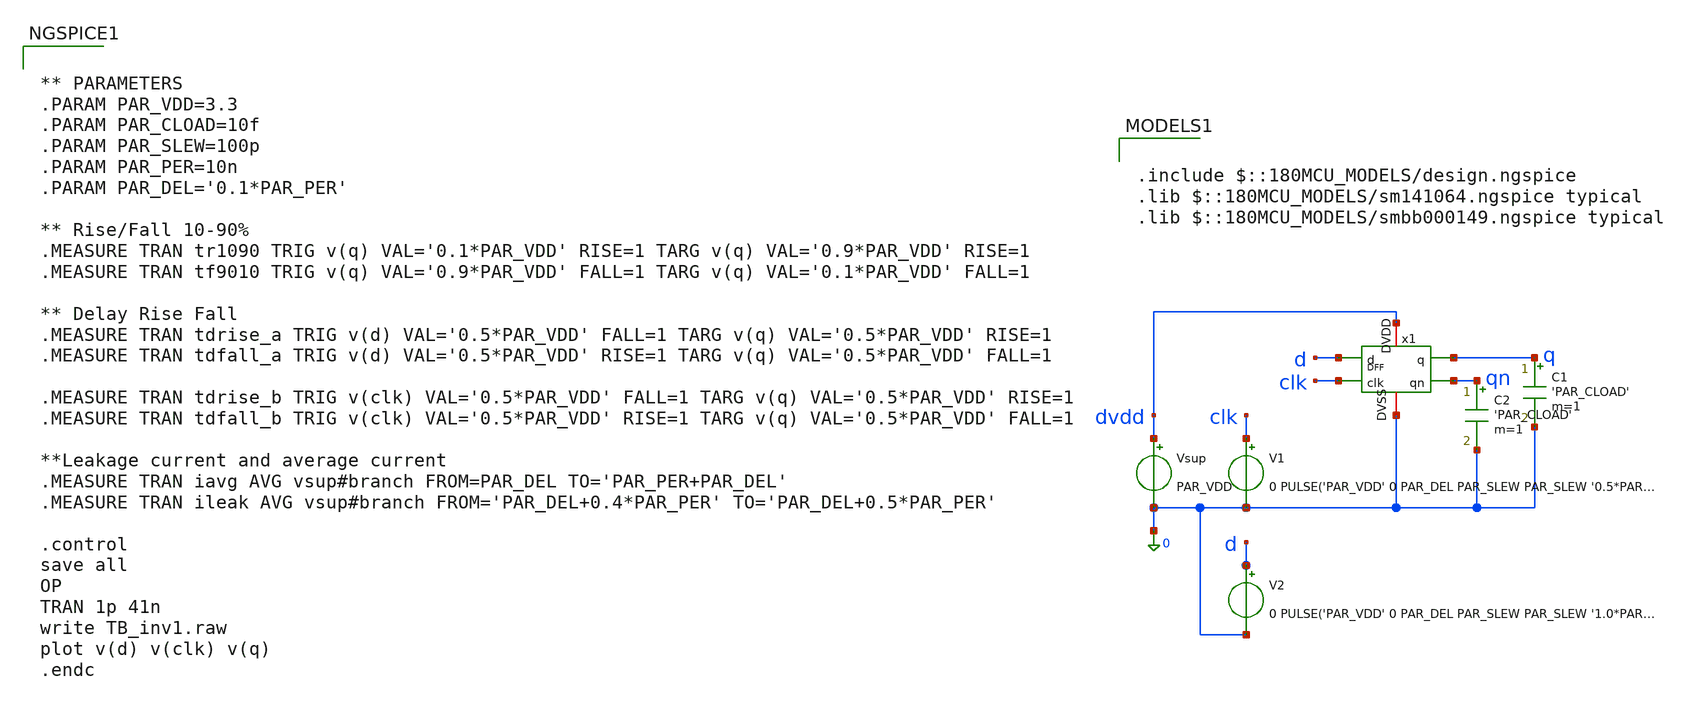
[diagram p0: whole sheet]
** sch_path: src/schematic/DFF/TB_DFF.sch
**.subckt TB_DFF
V1 clk 0 0 PULSE('PAR_VDD' 0 PAR_DEL PAR_SLEW PAR_SLEW '0.5*PAR_PER' '1.0*PAR_PER')
Vsup dvdd 0 PAR_VDD
C1 q 0 'PAR_CLOAD' m=1
V2 d 0 0 PULSE('PAR_VDD' 0 PAR_DEL PAR_SLEW PAR_SLEW '1.0*PAR_PER' '2.0*PAR_PER')
C2 qn 0 'PAR_CLOAD' m=1
x1 d q clk dvdd qn 0 DFF
**** begin user architecture code

.include $::180MCU_MODELS/design.ngspice
.lib $::180MCU_MODELS/sm141064.ngspice typical
.lib $::180MCU_MODELS/smbb000149.ngspice typical



** PARAMETERS
.PARAM PAR_VDD=3.3
.PARAM PAR_CLOAD=10f
.PARAM PAR_SLEW=100p
.PARAM PAR_PER=10n
.PARAM PAR_DEL='0.1*PAR_PER'

** Rise/Fall 10-90%
.MEASURE TRAN tr1090 TRIG v(q) VAL='0.1*PAR_VDD' RISE=1 TARG v(q) VAL='0.9*PAR_VDD' RISE=1
.MEASURE TRAN tf9010 TRIG v(q) VAL='0.9*PAR_VDD' FALL=1 TARG v(q) VAL='0.1*PAR_VDD' FALL=1

** Delay Rise Fall
.MEASURE TRAN tdrise_a TRIG v(d) VAL='0.5*PAR_VDD' FALL=1 TARG v(q) VAL='0.5*PAR_VDD' RISE=1
.MEASURE TRAN tdfall_a TRIG v(d) VAL='0.5*PAR_VDD' RISE=1 TARG v(q) VAL='0.5*PAR_VDD' FALL=1

.MEASURE TRAN tdrise_b TRIG v(clk) VAL='0.5*PAR_VDD' FALL=1 TARG v(q) VAL='0.5*PAR_VDD' RISE=1
.MEASURE TRAN tdfall_b TRIG v(clk) VAL='0.5*PAR_VDD' RISE=1 TARG v(q) VAL='0.5*PAR_VDD' FALL=1

**Leakage current and average current
.MEASURE TRAN iavg AVG vsup#branch FROM=PAR_DEL TO='PAR_PER+PAR_DEL'
.MEASURE TRAN ileak AVG vsup#branch FROM='PAR_DEL+0.4*PAR_PER' TO='PAR_DEL+0.5*PAR_PER'

.control
save all
OP
TRAN 1p 41n
write TB_inv1.raw
plot v(d) v(clk) v(q)
.endc


**** end user architecture code
**.ends

* expanding   symbol:  Chipaton2026/src/schematic/DFF/DFF.sym # of pins=6
** sym_path: src/schematic/DFF/DFF.sym
** sch_path: src/schematic/DFF/DFF.sch
.subckt DFF d q clk DVDD qn DVSS
*.ipin d
*.ipin clk
*.iopin DVDD
*.iopin DVSS
*.opin q
*.opin qn
x1 d net3 net1 DVDD net4 DVSS DLATCH
x2 DVDD clk net1 DVSS Inv1
x3 net3 q net2 DVDD qn DVSS DLATCH
x4 DVDD net1 net2 DVSS Inv1
* noconn #net4
.ends


* expanding   symbol:  src/schematic/DLATCH/DLATCH.sym # of pins=6
** sym_path: src/schematic/DLATCH/DLATCH.sym
** sch_path: src/schematic/DLATCH/DLATCH.sch
.subckt DLATCH d q e DVDD qn DVSS
*.ipin d
*.ipin e
*.iopin DVDD
*.iopin DVSS
*.opin q
*.opin qn
x1 DVDD net2 d e DVSS NAND
x2 DVDD net3 e net1 DVSS NAND
x3 DVDD q net2 qn DVSS NAND
x4 DVDD qn q net3 DVSS NAND
x5 DVDD d net1 DVSS Inv1
.ends


* expanding   symbol:  src/schematic/INV/Inv1.sym # of pins=4
** sym_path: src/schematic/INV/Inv1.sym
** sch_path: src/schematic/INV/Inv1.sch
.subckt Inv1 DVDD vin vout DVSS
*.ipin vin
*.opin vout
*.iopin DVDD
*.iopin DVSS
XM3 vout vin DVDD DVDD pfet_03v3 L=0.3u W=1.7u nf=1 ad='int((nf+1)/2) * W/nf * 0.18u' as='int((nf+2)/2) * W/nf * 0.18u'
+ pd='2*int((nf+1)/2) * (W/nf + 0.18u)' ps='2*int((nf+2)/2) * (W/nf + 0.18u)' nrd='0.18u / W' nrs='0.18u / W'
+ sa=0 sb=0 sd=0 m=1
XM4 vout vin DVSS DVSS nfet_03v3 L=0.3u W=0.85u nf=1 ad='int((nf+1)/2) * W/nf * 0.18u' as='int((nf+2)/2) * W/nf * 0.18u'
+ pd='2*int((nf+1)/2) * (W/nf + 0.18u)' ps='2*int((nf+2)/2) * (W/nf + 0.18u)' nrd='0.18u / W' nrs='0.18u / W'
+ sa=0 sb=0 sd=0 m=1
.ends


* expanding   symbol:  src/schematic/NAND/NAND.sym # of pins=5
** sym_path: src/schematic/NAND/NAND.sym
** sch_path: src/schematic/NAND/NAND.sch
.subckt NAND DVDD vout a b DVSS
*.ipin a
*.opin vout
*.iopin DVDD
*.iopin DVSS
*.ipin b
XM3 vout a DVDD DVDD pfet_03v3 L=0.3u W=1.7u nf=1 ad='int((nf+1)/2) * W/nf * 0.18u' as='int((nf+2)/2) * W/nf * 0.18u'
+ pd='2*int((nf+1)/2) * (W/nf + 0.18u)' ps='2*int((nf+2)/2) * (W/nf + 0.18u)' nrd='0.18u / W' nrs='0.18u / W'
+ sa=0 sb=0 sd=0 m=1
XM4 vout a net1 DVSS nfet_03v3 L=0.3u W=0.85u nf=1 ad='int((nf+1)/2) * W/nf * 0.18u' as='int((nf+2)/2) * W/nf * 0.18u'
+ pd='2*int((nf+1)/2) * (W/nf + 0.18u)' ps='2*int((nf+2)/2) * (W/nf + 0.18u)' nrd='0.18u / W' nrs='0.18u / W'
+ sa=0 sb=0 sd=0 m=1
XM1 vout b DVDD DVDD pfet_03v3 L=0.3u W=1.7u nf=1 ad='int((nf+1)/2) * W/nf * 0.18u' as='int((nf+2)/2) * W/nf * 0.18u'
+ pd='2*int((nf+1)/2) * (W/nf + 0.18u)' ps='2*int((nf+2)/2) * (W/nf + 0.18u)' nrd='0.18u / W' nrs='0.18u / W'
+ sa=0 sb=0 sd=0 m=1
XM2 net1 b DVSS DVSS nfet_03v3 L=0.3u W=0.85u nf=1 ad='int((nf+1)/2) * W/nf * 0.18u' as='int((nf+2)/2) * W/nf * 0.18u'
+ pd='2*int((nf+1)/2) * (W/nf + 0.18u)' ps='2*int((nf+2)/2) * (W/nf + 0.18u)' nrd='0.18u / W' nrs='0.18u / W'
+ sa=0 sb=0 sd=0 m=1
.ends

.end
